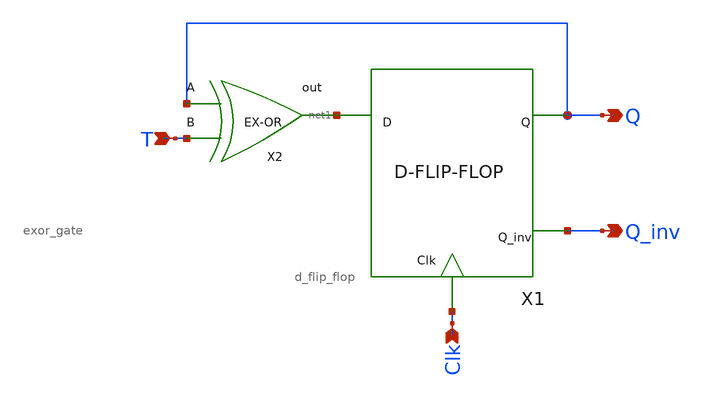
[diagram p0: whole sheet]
** sch_path: xschem/T_flip_flop/T_flip_flop.sch
**.subckt T_flip_flop T Clk Q Q_inv
*.ipin T
*.ipin Clk
*.opin Q
*.opin Q_inv
X1 net1 Q Q_inv Clk d_flip_flop
X2 Q T net1 exor_gate
**.ends

* expanding   symbol:  D_flip_flop/d_flip_flop.sym # of pins=4
** sym_path: xschem/D_flip_flop/d_flip_flop.sym
** sch_path: xschem/D_flip_flop/d_flip_flop.sch
.subckt d_flip_flop D Q Q_inv Clk
*.ipin D
*.ipin Clk
*.opin Q_inv
*.opin Q
X1 net1 net2 inv Wpmos=3 Lpmos=0.18 Wnmos=1 Lnmos=0.18
X2 net3 Q inv Wpmos=3 Lpmos=0.18 Wnmos=1 Lnmos=0.18
X3 net2 net4 inv Wpmos=3 Lpmos=0.18 Wnmos=1 Lnmos=0.18
X4 Q Q_inv inv Wpmos=3 Lpmos=0.18 Wnmos=1 Lnmos=0.18
X5 D net1 Clk Clk_inv transmission_gate Wpmos=1 Lpmos=0.18 Wnmos=1 Lnmos=0.18
X6 net1 net4 Clk_inv Clk transmission_gate Wpmos=1 Lpmos=0.18 Wnmos=1 Lnmos=0.18
X7 net3 Q_inv Clk Clk_inv transmission_gate Wpmos=1 Lpmos=0.18 Wnmos=1 Lnmos=0.18
X8 net2 net3 Clk_inv Clk transmission_gate Wpmos=1 Lpmos=0.18 Wnmos=1 Lnmos=0.18
X9 Clk Clk_inv inv Wpmos=3 Lpmos=0.18 Wnmos=1 Lnmos=0.18
.ends


* expanding   symbol:  exor_gate/exor_gate.sym # of pins=3
** sym_path: xschem/exor_gate/exor_gate.sym
** sch_path: xschem/exor_gate/exor_gate.sch
.subckt exor_gate A B out
*.ipin A
*.ipin B
*.opin out
XM4 out A net1 GND sky130_fd_pr__nfet_01v8 L=0.18 W=0.5 nf=1 ad='int((nf+1)/2) * W/nf * 0.29' as='int((nf+2)/2) * W/nf * 0.29'
+ pd='2*int((nf+1)/2) * (W/nf + 0.29)' ps='2*int((nf+2)/2) * (W/nf + 0.29)' nrd='0.29 / W' nrs='0.29 / W'
+ sa=0 sb=0 sd=0 mult=1 m=1
XM5 net3 B VDD VDD sky130_fd_pr__pfet_01v8 L=0.18 W=1 nf=1 ad='int((nf+1)/2) * W/nf * 0.29' as='int((nf+2)/2) * W/nf * 0.29'
+ pd='2*int((nf+1)/2) * (W/nf + 0.29)' ps='2*int((nf+2)/2) * (W/nf + 0.29)' nrd='0.29 / W' nrs='0.29 / W'
+ sa=0 sb=0 sd=0 mult=1 m=1
XM1 net1 B GND GND sky130_fd_pr__nfet_01v8 L=0.18 W=0.5 nf=1 ad='int((nf+1)/2) * W/nf * 0.29' as='int((nf+2)/2) * W/nf * 0.29'
+ pd='2*int((nf+1)/2) * (W/nf + 0.29)' ps='2*int((nf+2)/2) * (W/nf + 0.29)' nrd='0.29 / W' nrs='0.29 / W'
+ sa=0 sb=0 sd=0 mult=1 m=1
XM2 out net5 net3 VDD sky130_fd_pr__pfet_01v8 L=0.18 W=1 nf=1 ad='int((nf+1)/2) * W/nf * 0.29' as='int((nf+2)/2) * W/nf * 0.29'
+ pd='2*int((nf+1)/2) * (W/nf + 0.29)' ps='2*int((nf+2)/2) * (W/nf + 0.29)' nrd='0.29 / W' nrs='0.29 / W'
+ sa=0 sb=0 sd=0 mult=1 m=1
XM3 net4 net6 VDD VDD sky130_fd_pr__pfet_01v8 L=0.18 W=1 nf=1 ad='int((nf+1)/2) * W/nf * 0.29' as='int((nf+2)/2) * W/nf * 0.29'
+ pd='2*int((nf+1)/2) * (W/nf + 0.29)' ps='2*int((nf+2)/2) * (W/nf + 0.29)' nrd='0.29 / W' nrs='0.29 / W'
+ sa=0 sb=0 sd=0 mult=1 m=1
XM6 out A net4 VDD sky130_fd_pr__pfet_01v8 L=0.18 W=1 nf=1 ad='int((nf+1)/2) * W/nf * 0.29' as='int((nf+2)/2) * W/nf * 0.29'
+ pd='2*int((nf+1)/2) * (W/nf + 0.29)' ps='2*int((nf+2)/2) * (W/nf + 0.29)' nrd='0.29 / W' nrs='0.29 / W'
+ sa=0 sb=0 sd=0 mult=1 m=1
XM7 out net5 net2 GND sky130_fd_pr__nfet_01v8 L=0.18 W=0.5 nf=1 ad='int((nf+1)/2) * W/nf * 0.29' as='int((nf+2)/2) * W/nf * 0.29'
+ pd='2*int((nf+1)/2) * (W/nf + 0.29)' ps='2*int((nf+2)/2) * (W/nf + 0.29)' nrd='0.29 / W' nrs='0.29 / W'
+ sa=0 sb=0 sd=0 mult=1 m=1
XM8 net2 net6 GND GND sky130_fd_pr__nfet_01v8 L=0.18 W=0.5 nf=1 ad='int((nf+1)/2) * W/nf * 0.29' as='int((nf+2)/2) * W/nf * 0.29'
+ pd='2*int((nf+1)/2) * (W/nf + 0.29)' ps='2*int((nf+2)/2) * (W/nf + 0.29)' nrd='0.29 / W' nrs='0.29 / W'
+ sa=0 sb=0 sd=0 mult=1 m=1
X3 B net6 inv Wpmos=3 Lpmos=0.18 Wnmos=1 Lnmos=0.18
X2 A net5 inv Wpmos=3 Lpmos=0.18 Wnmos=1 Lnmos=0.18
.ends


* expanding   symbol:  inv/inv.sym # of pins=2
** sym_path: xschem/inv/inv.sym
** sch_path: xschem/inv/inv.sch
.subckt inv in out  Wpmos=3 Lpmos=0.18 Wnmos=1 Lnmos=0.18
*.ipin in
*.iopin out
XM1 out in GND GND sky130_fd_pr__nfet_01v8 L=Lnmos W=Wnmos nf=1 ad='int((nf+1)/2) * W/nf * 0.29' as='int((nf+2)/2) * W/nf * 0.29'
+ pd='2*int((nf+1)/2) * (W/nf + 0.29)' ps='2*int((nf+2)/2) * (W/nf + 0.29)' nrd='0.29 / W' nrs='0.29 / W'
+ sa=0 sb=0 sd=0 mult=1 m=1
XM2 out in VDD VDD sky130_fd_pr__pfet_01v8 L=Lpmos W=Wpmos nf=1 ad='int((nf+1)/2) * W/nf * 0.29' as='int((nf+2)/2) * W/nf * 0.29'
+ pd='2*int((nf+1)/2) * (W/nf + 0.29)' ps='2*int((nf+2)/2) * (W/nf + 0.29)' nrd='0.29 / W' nrs='0.29 / W'
+ sa=0 sb=0 sd=0 mult=1 m=1
.ends


* expanding   symbol:  transmission_gate/transmission_gate.sym # of pins=4
** sym_path: xschem/transmission_gate/transmission_gate.sym
** sch_path: xschem/transmission_gate/transmission_gate.sch
.subckt transmission_gate in out ctrl_ ctrl  Wpmos=1 Lpmos=0.18 Wnmos=1 Lnmos=0.18
*.iopin in
*.iopin out
*.ipin ctrl_
*.ipin ctrl
XM1 in ctrl out GND sky130_fd_pr__nfet_01v8 L=Lnmos W=Wnmos nf=1 ad='int((nf+1)/2) * W/nf * 0.29' as='int((nf+2)/2) * W/nf * 0.29'
+ pd='2*int((nf+1)/2) * (W/nf + 0.29)' ps='2*int((nf+2)/2) * (W/nf + 0.29)' nrd='0.29 / W' nrs='0.29 / W'
+ sa=0 sb=0 sd=0 mult=1 m=1
XM2 out ctrl_ in VDD sky130_fd_pr__pfet_01v8 L=Lpmos W=Wpmos nf=1 ad='int((nf+1)/2) * W/nf * 0.29' as='int((nf+2)/2) * W/nf * 0.29'
+ pd='2*int((nf+1)/2) * (W/nf + 0.29)' ps='2*int((nf+2)/2) * (W/nf + 0.29)' nrd='0.29 / W' nrs='0.29 / W'
+ sa=0 sb=0 sd=0 mult=1 m=1
.ends

.GLOBAL VDD
.GLOBAL GND
.end
